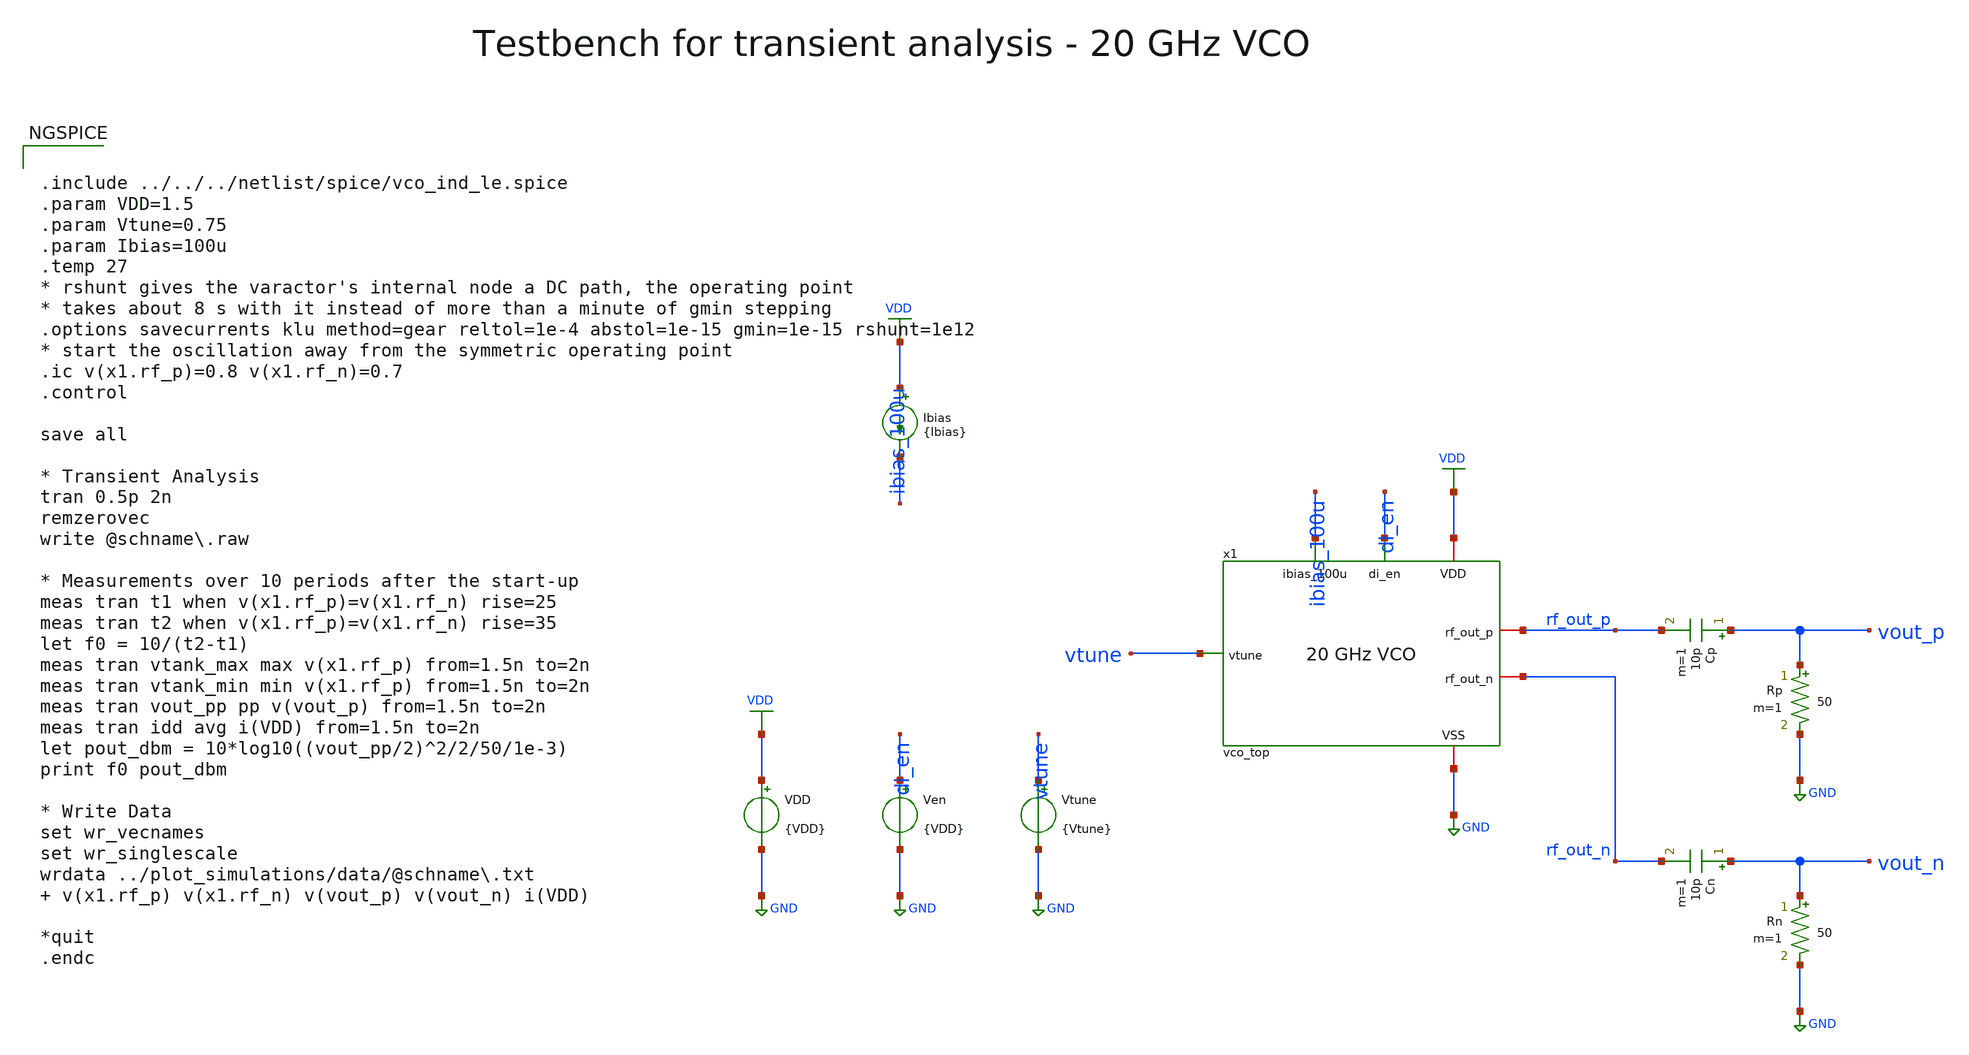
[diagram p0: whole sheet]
** sch_path: macros/vco/testbenches/xschem/vco_top_tb_tran.sch
**.subckt vco_top_tb_tran
x1 ibias_100u di_en VDD GND vtune rf_out_p rf_out_n vco_top
Cp vout_p rf_out_p 10p m=1
Rp vout_p GND 50 m=1
Cn vout_n rf_out_n 10p m=1
Rn vout_n GND 50 m=1
VDD VDD GND {VDD}
Ven di_en GND {VDD}
Vtune vtune GND {Vtune}
Ibias VDD ibias_100u {Ibias}
**** begin user architecture code


.include ../../../netlist/spice/vco_ind_le.spice
.param VDD=1.5
.param Vtune=0.75
.param Ibias=100u
.temp 27
* rshunt gives the varactor's internal node a DC path, the operating point
* takes about 8 s with it instead of more than a minute of gmin stepping
.options savecurrents klu method=gear reltol=1e-4 abstol=1e-15 gmin=1e-15 rshunt=1e12
* start the oscillation away from the symmetric operating point
.ic v(x1.rf_p)=0.8 v(x1.rf_n)=0.7
.control

save all

* Transient Analysis
tran 0.5p 2n
remzerovec
write @schname\.raw

* Measurements over 10 periods after the start-up
meas tran t1 when v(x1.rf_p)=v(x1.rf_n) rise=25
meas tran t2 when v(x1.rf_p)=v(x1.rf_n) rise=35
let f0 = 10/(t2-t1)
meas tran vtank_max max v(x1.rf_p) from=1.5n to=2n
meas tran vtank_min min v(x1.rf_p) from=1.5n to=2n
meas tran vout_pp pp v(vout_p) from=1.5n to=2n
meas tran idd avg i(VDD) from=1.5n to=2n
let pout_dbm = 10*log10((vout_pp/2)^2/2/50/1e-3)
print f0 pout_dbm

* Write Data
set wr_vecnames
set wr_singlescale
wrdata ../plot_simulations/data/@schname\.txt  v(x1.rf_p) v(x1.rf_n) v(vout_p) v(vout_n) i(VDD)

*quit
.endc



.lib cornerMOSlv.lib mos_tt
.lib cornerMOShv.lib mos_tt
.lib cornerRES.lib res_typ
.lib cornerCAP.lib cap_typ

**** end user architecture code
**.ends

* expanding   symbol:  vco_top.sym # of pins=7
** sym_path: macros/vco/schematic/xschem/vco_top.sym
** sch_path: macros/vco/schematic/xschem/vco_top.sch
.subckt vco_top ibias_100u di_en VDD VSS vtune rf_out_p rf_out_n
*.iopin VDD
*.iopin VSS
*.ipin ibias_100u
*.ipin di_en
*.ipin vtune
*.iopin rf_out_p
*.iopin rf_out_n
xbias ibias_100u di_en VDD VSS vbg_buf vbn_buf vbp_core vco_bias
xcore vbp_core VDD VSS vtune rf_p rf_n vco_core
xbuf vbn_buf vbg_buf VDD VSS rf_p rf_n rf_out_p rf_out_n vco_buf
.ends


* expanding   symbol:  vco_bias.sym # of pins=7
** sym_path: macros/vco/schematic/xschem/vco_bias.sym
** sch_path: macros/vco/schematic/xschem/vco_bias.sch
.subckt vco_bias ibias_100u di_en VDD VSS vbg_buf vbn_buf vbp_core
*.iopin VDD
*.iopin VSS
*.ipin di_en
*.ipin ibias_100u
*.iopin vbn_buf
*.iopin vbp_core
*.iopin vbg_buf
XMPi1 en_b di_en VDD VDD sg13_lv_pmos w=1u l=0.13u ng=1 m=1 mm_ok=1
XMNi1 en_b di_en VSS VSS sg13_lv_nmos w=0.5u l=0.13u ng=1 m=1 mm_ok=1
XMPi2 en en_b VDD VDD sg13_lv_pmos w=1u l=0.13u ng=1 m=1 mm_ok=1
XMNi2 en en_b VSS VSS sg13_lv_nmos w=0.5u l=0.13u ng=1 m=1 mm_ok=1
XMN0 ibias_100u ibias_100u VSS VSS sg13_lv_nmos w=2.5u l=0.5u ng=1 m=1 mm_ok=1
XMNd0 ibias_100u en_b VSS VSS sg13_lv_nmos w=1u l=0.13u ng=1 m=1 mm_ok=1
XRn ibias_100u vbn_buf VSS rhigh w=0.5e-6 l=16e-6 m=1 b=0 mm_ok=1
XCn vbn_buf VSS cap_cmim w=30e-6 l=30e-6 m=1 mm_ok=1
XMNd1 vbn_buf en_b VSS VSS sg13_lv_nmos w=1u l=0.13u ng=1 m=1 mm_ok=1
XMN1 vbp_ref ibias_100u VSS VSS sg13_lv_nmos w=2.5u l=0.5u ng=1 m=1 mm_ok=1
XMP1 vbp_ref vbp_ref VDD VDD sg13_lv_pmos w=5u l=0.5u ng=1 m=1 mm_ok=1
XRp vbp_ref vbp_core VSS rhigh w=0.5e-6 l=16e-6 m=1 b=0 mm_ok=1
XCp VDD vbp_core cap_cmim w=30e-6 l=30e-6 m=1 mm_ok=1
XMPd vbp_core en VDD VDD sg13_lv_pmos w=1u l=0.13u ng=1 m=1 mm_ok=1
XMP2 vbg_buf vbp_core VDD VDD sg13_lv_pmos w=5u l=0.5u ng=1 m=1 mm_ok=1
XRg vbg_buf nbg VSS rppd w=0.5e-6 l=8.5e-6 m=1 b=0 mm_ok=1
XMN3 nbg nbg VSS VSS sg13_lv_nmos w=2.5u l=0.5u ng=1 m=1 mm_ok=1
XCg vbg_buf VSS cap_cmim w=20e-6 l=20e-6 m=1 mm_ok=1
.ends


* expanding   symbol:  vco_core.sym # of pins=6
** sym_path: macros/vco/schematic/xschem/vco_core.sym
** sch_path: macros/vco/schematic/xschem/vco_core.sch
.subckt vco_core vbp_core VDD VSS vtune rf_p rf_n
*.iopin VDD
*.iopin VSS
*.ipin vbp_core
*.ipin vtune
*.iopin rf_p
*.iopin rf_n
XMtop vct vbp_core VDD VDD sg13_lv_pmos w=150u l=0.5u ng=30 m=1 mm_ok=1
xind rf_p rf_n vct VSS vco_ind
XCct vct VSS cap_cmim w=25e-6 l=25e-6 m=1 mm_ok=1
xvar rf_p rf_n vtune VSS vco_var
XM1 rf_p rf_n VSS VSS sg13_lv_nmos w=20u l=0.13u ng=10 m=1 mm_ok=1
XM2 rf_n rf_p VSS VSS sg13_lv_nmos w=20u l=0.13u ng=10 m=1 mm_ok=1
.ends


* expanding   symbol:  vco_buf.sym # of pins=8
** sym_path: macros/vco/schematic/xschem/vco_buf.sym
** sch_path: macros/vco/schematic/xschem/vco_buf.sch
.subckt vco_buf vbn_buf vbg_buf VDD VSS rf_p rf_n rf_out_p rf_out_n
*.iopin VDD
*.iopin VSS
*.iopin rf_out_n
*.iopin rf_out_p
*.ipin vbn_buf
*.iopin rf_p
*.iopin rf_n
*.ipin vbg_buf
XMB1 rf_out_n gp tail VSS sg13_lv_nmos w=24u l=0.13u ng=12 m=1 mm_ok=1
XMB2 rf_out_p gn tail VSS sg13_lv_nmos w=24u l=0.13u ng=12 m=1 mm_ok=1
XRL1 VDD rf_out_n VSS rppd w=10e-6 l=1.65e-6 m=1 b=0 mm_ok=1
XRL2 VDD rf_out_p VSS rppd w=10e-6 l=1.65e-6 m=1 b=0 mm_ok=1
XMBt tail vbn_buf VSS VSS sg13_lv_nmos w=150u l=0.5u ng=30 m=1 mm_ok=1
XCc1 gp rf_p cap_cmim w=10e-6 l=10e-6 m=1 mm_ok=1
XCc2 gn rf_n cap_cmim w=10e-6 l=10e-6 m=1 mm_ok=1
XRb1 vbg_buf gp VSS rhigh w=0.5e-6 l=8e-6 m=1 b=0 mm_ok=1
XRb2 vbg_buf gn VSS rhigh w=0.5e-6 l=8e-6 m=1 b=0 mm_ok=1
.ends


* expanding   symbol:  vco_ind.sym # of pins=4
** sym_path: macros/vco/schematic/xschem/vco_ind.sym
** sch_path: macros/vco/schematic/xschem/vco_ind.sch
.subckt vco_ind la lb lc VSS
*.iopin la
*.iopin lc
*.iopin lb
*.iopin VSS
XL1 la lc lb VSS inductor3 w=4e-6 s=4e-6 d=52e-6 nr_r=2 m=1
x1 la lb lc vco_ind_le
.ends


* expanding   symbol:  vco_var.sym # of pins=4
** sym_path: macros/vco/schematic/xschem/vco_var.sym
** sch_path: macros/vco/schematic/xschem/vco_var.sch
.subckt vco_var rf_p rf_n vtune VSS
*.ipin vtune
*.iopin rf_p
*.iopin rf_n
*.iopin VSS
XCvar1 rf_p vtune rf_n VSS sg13_hv_svaricap w=3.74u l=0.3u Nx=7 mm_ok=1
XCvar2 rf_p vtune rf_n VSS sg13_hv_svaricap w=3.74u l=0.3u Nx=7 mm_ok=1
XCvar3 rf_p vtune rf_n VSS sg13_hv_svaricap w=3.74u l=0.3u Nx=7 mm_ok=1
.ends

.GLOBAL VDD
.GLOBAL GND
.end
